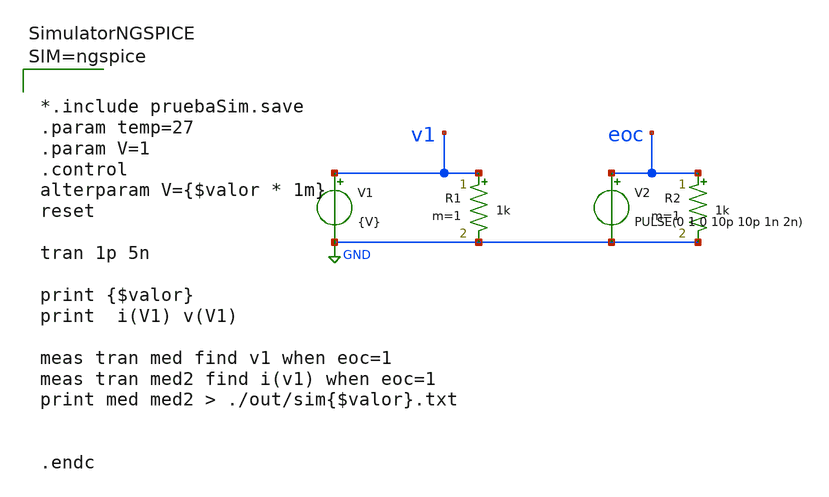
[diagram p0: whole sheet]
** sch_path: pruebaSim/plantillaPrueba.sch
**.subckt plantillaPrueba
V1 v1 GND {V}
R1 v1 GND 1k m=1
V2 eoc GND PULSE(0 1 0 10p 10p 1n 2n)
R2 eoc GND 1k m=1
**** begin user architecture code



*.include pruebaSim.save
.param temp=27
.param V=1
.control
alterparam V={$valor * 1m}
reset

tran 1p 5n

print {$valor}
print  i(V1) v(V1)

meas tran med find v1 when eoc=1
meas tran med2 find i(v1) when eoc=1
print med med2 > ./out/sim{$valor}.txt


.endc



**** end user architecture code
**.ends
.GLOBAL GND
.end
